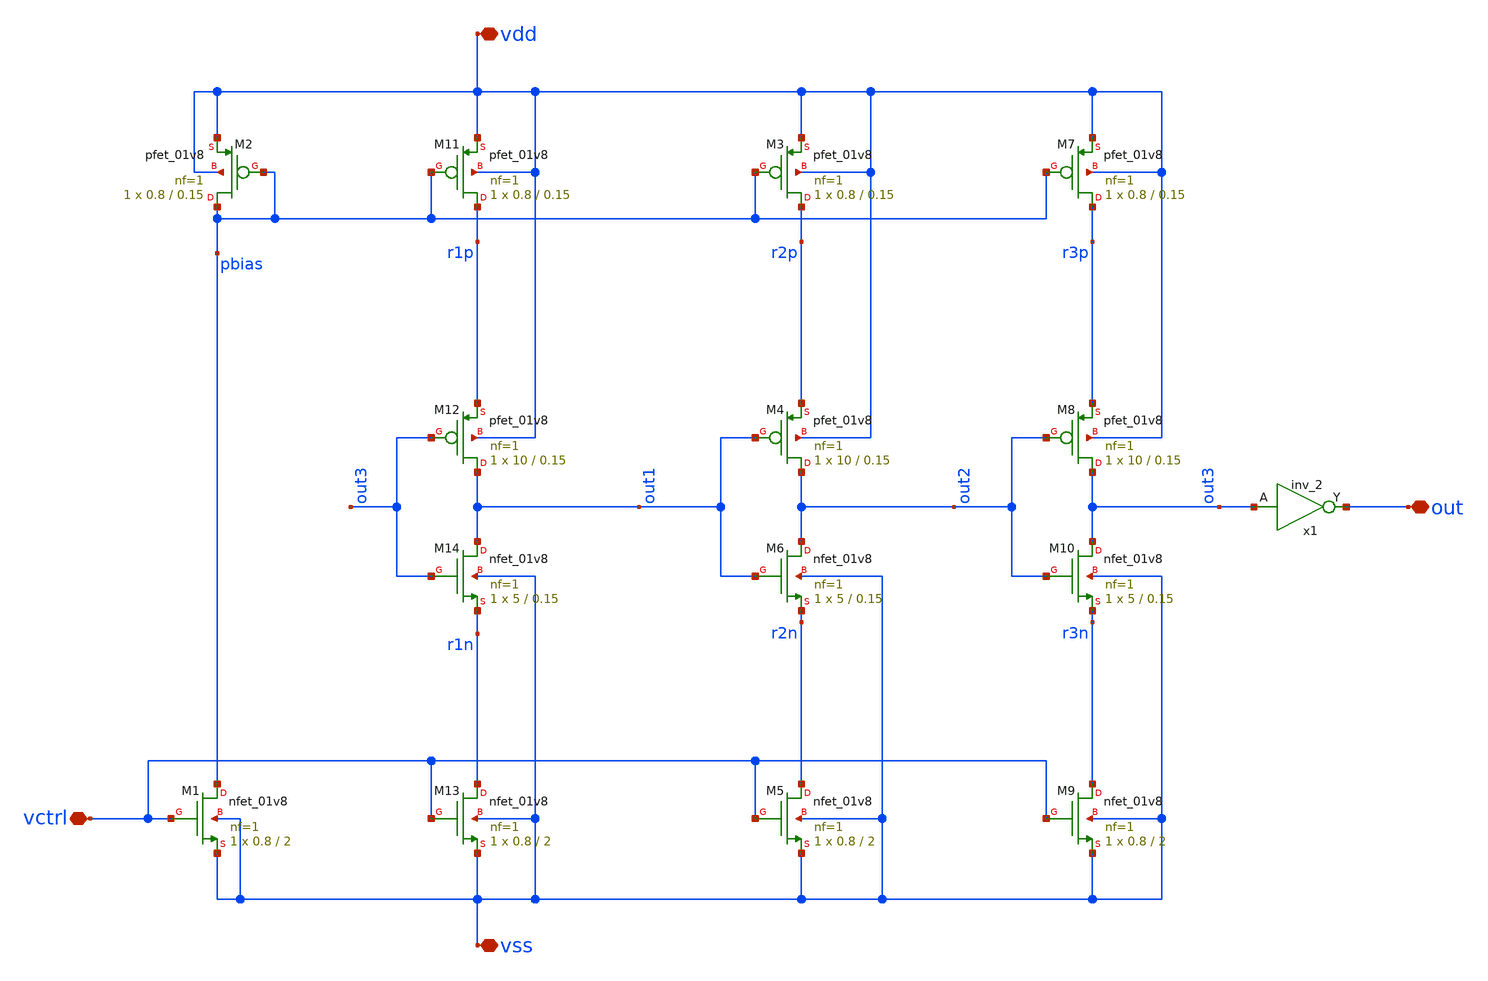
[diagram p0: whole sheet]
** sch_path: xschem/vco/VCO_Final.sch
**.subckt VCO_Final vdd vss vctrl out
*.iopin vdd
*.iopin vss
*.iopin vctrl
*.iopin out
XM1 pbias vctrl vss vss sky130_fd_pr__nfet_01v8 L=2 W=0.8 nf=1 ad='int((nf+1)/2) * W/nf * 0.29' as='int((nf+2)/2) * W/nf * 0.29'
+ pd='2*int((nf+1)/2) * (W/nf + 0.29)' ps='2*int((nf+2)/2) * (W/nf + 0.29)' nrd='0.29 / W' nrs='0.29 / W'
+ sa=0 sb=0 sd=0 mult=1 m=1
XM2 pbias pbias vdd vdd sky130_fd_pr__pfet_01v8 L=0.15 W=0.8 nf=1 ad='int((nf+1)/2) * W/nf * 0.29' as='int((nf+2)/2) * W/nf * 0.29'
+ pd='2*int((nf+1)/2) * (W/nf + 0.29)' ps='2*int((nf+2)/2) * (W/nf + 0.29)' nrd='0.29 / W' nrs='0.29 / W'
+ sa=0 sb=0 sd=0 mult=1 m=1
XM11 r1p pbias vdd vdd sky130_fd_pr__pfet_01v8 L=0.15 W=0.8 nf=1 ad='int((nf+1)/2) * W/nf * 0.29' as='int((nf+2)/2) * W/nf * 0.29'
+ pd='2*int((nf+1)/2) * (W/nf + 0.29)' ps='2*int((nf+2)/2) * (W/nf + 0.29)' nrd='0.29 / W' nrs='0.29 / W'
+ sa=0 sb=0 sd=0 mult=1 m=1
XM12 out1 out3 r1p vdd sky130_fd_pr__pfet_01v8 L=0.15 W=10 nf=1 ad='int((nf+1)/2) * W/nf * 0.29' as='int((nf+2)/2) * W/nf * 0.29'
+ pd='2*int((nf+1)/2) * (W/nf + 0.29)' ps='2*int((nf+2)/2) * (W/nf + 0.29)' nrd='0.29 / W' nrs='0.29 / W'
+ sa=0 sb=0 sd=0 mult=1 m=1
XM13 r1n vctrl vss vss sky130_fd_pr__nfet_01v8 L=2 W=0.8 nf=1 ad='int((nf+1)/2) * W/nf * 0.29' as='int((nf+2)/2) * W/nf * 0.29'
+ pd='2*int((nf+1)/2) * (W/nf + 0.29)' ps='2*int((nf+2)/2) * (W/nf + 0.29)' nrd='0.29 / W' nrs='0.29 / W'
+ sa=0 sb=0 sd=0 mult=1 m=1
XM14 out1 out3 r1n vss sky130_fd_pr__nfet_01v8 L=0.15 W=5 nf=1 ad='int((nf+1)/2) * W/nf * 0.29' as='int((nf+2)/2) * W/nf * 0.29'
+ pd='2*int((nf+1)/2) * (W/nf + 0.29)' ps='2*int((nf+2)/2) * (W/nf + 0.29)' nrd='0.29 / W' nrs='0.29 / W'
+ sa=0 sb=0 sd=0 mult=1 m=1
x1 out3 vss vss vdd vdd out sky130_fd_sc_hd__inv_2
XM3 r2p pbias vdd vdd sky130_fd_pr__pfet_01v8 L=0.15 W=0.8 nf=1 ad='int((nf+1)/2) * W/nf * 0.29' as='int((nf+2)/2) * W/nf * 0.29'
+ pd='2*int((nf+1)/2) * (W/nf + 0.29)' ps='2*int((nf+2)/2) * (W/nf + 0.29)' nrd='0.29 / W' nrs='0.29 / W'
+ sa=0 sb=0 sd=0 mult=1 m=1
XM4 out2 out1 r2p vdd sky130_fd_pr__pfet_01v8 L=0.15 W=10 nf=1 ad='int((nf+1)/2) * W/nf * 0.29' as='int((nf+2)/2) * W/nf * 0.29'
+ pd='2*int((nf+1)/2) * (W/nf + 0.29)' ps='2*int((nf+2)/2) * (W/nf + 0.29)' nrd='0.29 / W' nrs='0.29 / W'
+ sa=0 sb=0 sd=0 mult=1 m=1
XM5 r2n vctrl vss vss sky130_fd_pr__nfet_01v8 L=2 W=0.8 nf=1 ad='int((nf+1)/2) * W/nf * 0.29' as='int((nf+2)/2) * W/nf * 0.29'
+ pd='2*int((nf+1)/2) * (W/nf + 0.29)' ps='2*int((nf+2)/2) * (W/nf + 0.29)' nrd='0.29 / W' nrs='0.29 / W'
+ sa=0 sb=0 sd=0 mult=1 m=1
XM6 out2 out1 r2n vss sky130_fd_pr__nfet_01v8 L=0.15 W=5 nf=1 ad='int((nf+1)/2) * W/nf * 0.29' as='int((nf+2)/2) * W/nf * 0.29'
+ pd='2*int((nf+1)/2) * (W/nf + 0.29)' ps='2*int((nf+2)/2) * (W/nf + 0.29)' nrd='0.29 / W' nrs='0.29 / W'
+ sa=0 sb=0 sd=0 mult=1 m=1
XM7 r3p pbias vdd vdd sky130_fd_pr__pfet_01v8 L=0.15 W=0.8 nf=1 ad='int((nf+1)/2) * W/nf * 0.29' as='int((nf+2)/2) * W/nf * 0.29'
+ pd='2*int((nf+1)/2) * (W/nf + 0.29)' ps='2*int((nf+2)/2) * (W/nf + 0.29)' nrd='0.29 / W' nrs='0.29 / W'
+ sa=0 sb=0 sd=0 mult=1 m=1
XM8 out3 out2 r3p vdd sky130_fd_pr__pfet_01v8 L=0.15 W=10 nf=1 ad='int((nf+1)/2) * W/nf * 0.29' as='int((nf+2)/2) * W/nf * 0.29'
+ pd='2*int((nf+1)/2) * (W/nf + 0.29)' ps='2*int((nf+2)/2) * (W/nf + 0.29)' nrd='0.29 / W' nrs='0.29 / W'
+ sa=0 sb=0 sd=0 mult=1 m=1
XM9 r3n vctrl vss vss sky130_fd_pr__nfet_01v8 L=2 W=0.8 nf=1 ad='int((nf+1)/2) * W/nf * 0.29' as='int((nf+2)/2) * W/nf * 0.29'
+ pd='2*int((nf+1)/2) * (W/nf + 0.29)' ps='2*int((nf+2)/2) * (W/nf + 0.29)' nrd='0.29 / W' nrs='0.29 / W'
+ sa=0 sb=0 sd=0 mult=1 m=1
XM10 out3 out2 r3n vss sky130_fd_pr__nfet_01v8 L=0.15 W=5 nf=1 ad='int((nf+1)/2) * W/nf * 0.29' as='int((nf+2)/2) * W/nf * 0.29'
+ pd='2*int((nf+1)/2) * (W/nf + 0.29)' ps='2*int((nf+2)/2) * (W/nf + 0.29)' nrd='0.29 / W' nrs='0.29 / W'
+ sa=0 sb=0 sd=0 mult=1 m=1
**.ends
.end
